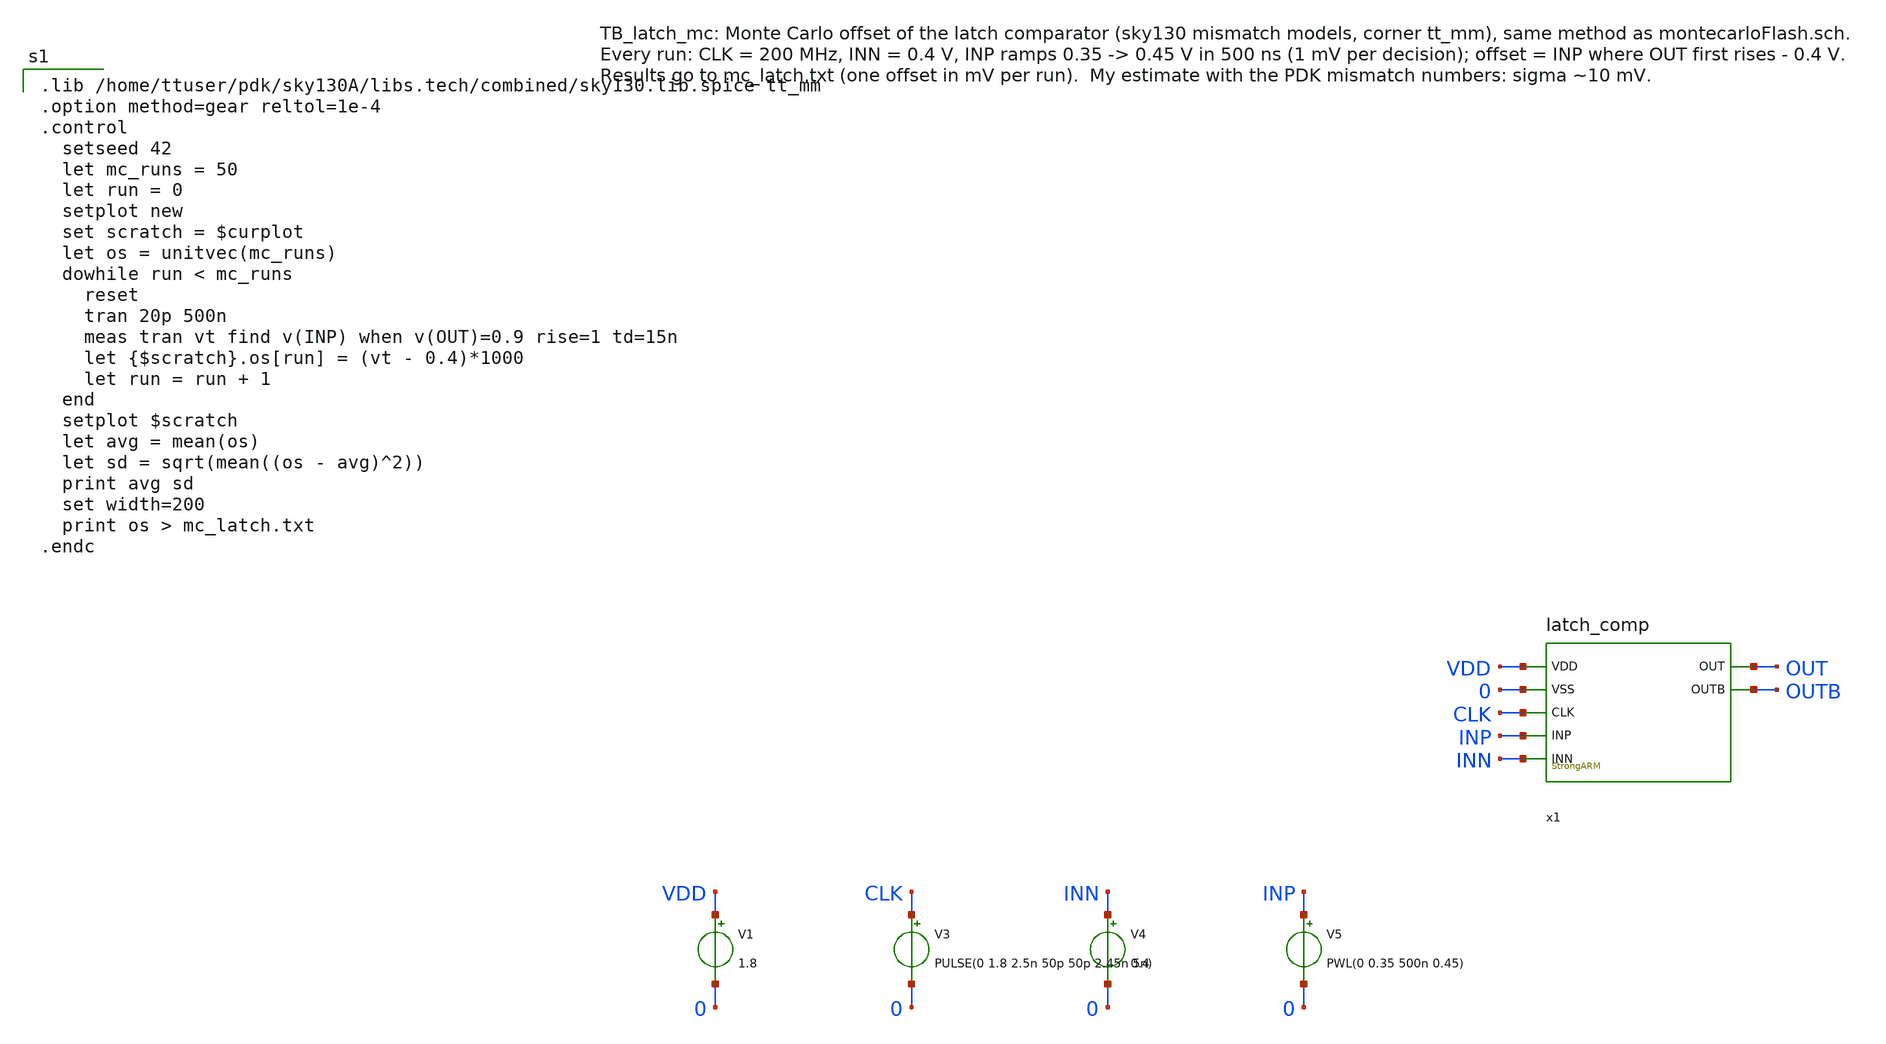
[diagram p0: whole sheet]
** sch_path: TB_latch_mc.sch
**.subckt TB_latch_mc
x1 VDD 0 CLK INP INN OUT OUTB latch_comp
V1 VDD 0 1.8
V3 CLK 0 PULSE(0 1.8 2.5n 50p 50p 2.45n 5n)
V4 INN 0 0.4
V5 INP 0 PWL(0 0.35 500n 0.45)
**** begin user architecture code

.lib /home/ttuser/pdk/sky130A/libs.tech/combined/sky130.lib.spice tt_mm
.option method=gear reltol=1e-4
.control
  setseed 42
  let mc_runs = 50
  let run = 0
  setplot new
  set scratch = $curplot
  let os = unitvec(mc_runs)
  dowhile run < mc_runs
    reset
    tran 20p 500n
    meas tran vt find v(INP) when v(OUT)=0.9 rise=1 td=15n
    let {$scratch}.os[run] = (vt - 0.4)*1000
    let run = run + 1
  end
  setplot $scratch
  let avg = mean(os)
  let sd = sqrt(mean((os - avg)^2))
  print avg sd
  set width=200
  print os > mc_latch.txt
.endc

**** end user architecture code
**.ends

* expanding   symbol:  /home/ttuser/Documents/ADCAnalogDesign/SAR_improved/latch_comp.sym # of
*+ pins=7
** sym_path: SAR_improved/latch_comp.sym
** sch_path: SAR_improved/latch_comp.sch
.subckt latch_comp VDD VSS CLK INP INN OUT OUTB
*.ipin VDD
*.ipin VSS
*.ipin CLK
*.ipin INP
*.ipin INN
*.opin OUT
*.opin OUTB
XM7 TAIL CLKB VDD VDD sky130_fd_pr__pfet_01v8 L=0.15 W=2 nf=1 ad='int((nf+1)/2) * W/nf * 0.29' as='int((nf+2)/2) * W/nf * 0.29'
+ pd='2*int((nf+1)/2) * (W/nf + 0.29)' ps='2*int((nf+2)/2) * (W/nf + 0.29)' nrd='0.29 / W' nrs='0.29 / W'
+ sa=0 sb=0 sd=0 mult=1 m=1
XM1 P INP TAIL VDD sky130_fd_pr__pfet_01v8 L=0.5 W=2 nf=1 ad='int((nf+1)/2) * W/nf * 0.29' as='int((nf+2)/2) * W/nf * 0.29'
+ pd='2*int((nf+1)/2) * (W/nf + 0.29)' ps='2*int((nf+2)/2) * (W/nf + 0.29)' nrd='0.29 / W' nrs='0.29 / W'
+ sa=0 sb=0 sd=0 mult=1 m=1
XM2 Q INN TAIL VDD sky130_fd_pr__pfet_01v8 L=0.5 W=2 nf=1 ad='int((nf+1)/2) * W/nf * 0.29' as='int((nf+2)/2) * W/nf * 0.29'
+ pd='2*int((nf+1)/2) * (W/nf + 0.29)' ps='2*int((nf+2)/2) * (W/nf + 0.29)' nrd='0.29 / W' nrs='0.29 / W'
+ sa=0 sb=0 sd=0 mult=1 m=1
XM3 X Y P VDD sky130_fd_pr__pfet_01v8 L=0.15 W=1 nf=1 ad='int((nf+1)/2) * W/nf * 0.29' as='int((nf+2)/2) * W/nf * 0.29'
+ pd='2*int((nf+1)/2) * (W/nf + 0.29)' ps='2*int((nf+2)/2) * (W/nf + 0.29)' nrd='0.29 / W' nrs='0.29 / W'
+ sa=0 sb=0 sd=0 mult=1 m=1
XM4 Y X Q VDD sky130_fd_pr__pfet_01v8 L=0.15 W=1 nf=1 ad='int((nf+1)/2) * W/nf * 0.29' as='int((nf+2)/2) * W/nf * 0.29'
+ pd='2*int((nf+1)/2) * (W/nf + 0.29)' ps='2*int((nf+2)/2) * (W/nf + 0.29)' nrd='0.29 / W' nrs='0.29 / W'
+ sa=0 sb=0 sd=0 mult=1 m=1
XM5 X Y VSS VSS sky130_fd_pr__nfet_01v8 L=0.15 W=0.5 nf=1 ad='int((nf+1)/2) * W/nf * 0.29' as='int((nf+2)/2) * W/nf * 0.29'
+ pd='2*int((nf+1)/2) * (W/nf + 0.29)' ps='2*int((nf+2)/2) * (W/nf + 0.29)' nrd='0.29 / W' nrs='0.29 / W'
+ sa=0 sb=0 sd=0 mult=1 m=1
XM6 Y X VSS VSS sky130_fd_pr__nfet_01v8 L=0.15 W=0.5 nf=1 ad='int((nf+1)/2) * W/nf * 0.29' as='int((nf+2)/2) * W/nf * 0.29'
+ pd='2*int((nf+1)/2) * (W/nf + 0.29)' ps='2*int((nf+2)/2) * (W/nf + 0.29)' nrd='0.29 / W' nrs='0.29 / W'
+ sa=0 sb=0 sd=0 mult=1 m=1
XMR1 P CLKB VSS VSS sky130_fd_pr__nfet_01v8 L=0.15 W=0.5 nf=1 ad='int((nf+1)/2) * W/nf * 0.29' as='int((nf+2)/2) * W/nf * 0.29'
+ pd='2*int((nf+1)/2) * (W/nf + 0.29)' ps='2*int((nf+2)/2) * (W/nf + 0.29)' nrd='0.29 / W' nrs='0.29 / W'
+ sa=0 sb=0 sd=0 mult=1 m=1
XMR2 Q CLKB VSS VSS sky130_fd_pr__nfet_01v8 L=0.15 W=0.5 nf=1 ad='int((nf+1)/2) * W/nf * 0.29' as='int((nf+2)/2) * W/nf * 0.29'
+ pd='2*int((nf+1)/2) * (W/nf + 0.29)' ps='2*int((nf+2)/2) * (W/nf + 0.29)' nrd='0.29 / W' nrs='0.29 / W'
+ sa=0 sb=0 sd=0 mult=1 m=1
XMR3 X CLKB VSS VSS sky130_fd_pr__nfet_01v8 L=0.15 W=0.5 nf=1 ad='int((nf+1)/2) * W/nf * 0.29' as='int((nf+2)/2) * W/nf * 0.29'
+ pd='2*int((nf+1)/2) * (W/nf + 0.29)' ps='2*int((nf+2)/2) * (W/nf + 0.29)' nrd='0.29 / W' nrs='0.29 / W'
+ sa=0 sb=0 sd=0 mult=1 m=1
XMR4 Y CLKB VSS VSS sky130_fd_pr__nfet_01v8 L=0.15 W=0.5 nf=1 ad='int((nf+1)/2) * W/nf * 0.29' as='int((nf+2)/2) * W/nf * 0.29'
+ pd='2*int((nf+1)/2) * (W/nf + 0.29)' ps='2*int((nf+2)/2) * (W/nf + 0.29)' nrd='0.29 / W' nrs='0.29 / W'
+ sa=0 sb=0 sd=0 mult=1 m=1
x1 YB OUTB OUT VDD VSS nand2
x2 XB OUT OUTB VDD VSS nand2
x3 VDD X XB VSS inverter
x4 VDD Y YB VSS inverter
x5 VDD CLK CLKB VSS inverter
.ends


* expanding   symbol:  /home/ttuser/Documents/ADCAnalogDesign/nand2.sym # of pins=5
** sym_path: nand2.sym
** sch_path: nand2.sch
.subckt nand2 A B Y VCC VSS
*.ipin A
*.ipin B
*.opin Y
*.iopin VCC
*.iopin VSS
XM1 Y A VCC VCC sky130_fd_pr__pfet_01v8 L=0.15 W=2 nf=1 ad='int((nf+1)/2) * W/nf * 0.29' as='int((nf+2)/2) * W/nf * 0.29'
+ pd='2*int((nf+1)/2) * (W/nf + 0.29)' ps='2*int((nf+2)/2) * (W/nf + 0.29)' nrd='0.29 / W' nrs='0.29 / W'
+ sa=0 sb=0 sd=0 mult=1 m=1
XM2 Y B VCC VCC sky130_fd_pr__pfet_01v8 L=0.15 W=2 nf=1 ad='int((nf+1)/2) * W/nf * 0.29' as='int((nf+2)/2) * W/nf * 0.29'
+ pd='2*int((nf+1)/2) * (W/nf + 0.29)' ps='2*int((nf+2)/2) * (W/nf + 0.29)' nrd='0.29 / W' nrs='0.29 / W'
+ sa=0 sb=0 sd=0 mult=1 m=1
XM3 Y A N1 VSS sky130_fd_pr__nfet_01v8 L=0.15 W=2 nf=1 ad='int((nf+1)/2) * W/nf * 0.29' as='int((nf+2)/2) * W/nf * 0.29'
+ pd='2*int((nf+1)/2) * (W/nf + 0.29)' ps='2*int((nf+2)/2) * (W/nf + 0.29)' nrd='0.29 / W' nrs='0.29 / W'
+ sa=0 sb=0 sd=0 mult=1 m=1
XM4 N1 B VSS VSS sky130_fd_pr__nfet_01v8 L=0.15 W=2 nf=1 ad='int((nf+1)/2) * W/nf * 0.29' as='int((nf+2)/2) * W/nf * 0.29'
+ pd='2*int((nf+1)/2) * (W/nf + 0.29)' ps='2*int((nf+2)/2) * (W/nf + 0.29)' nrd='0.29 / W' nrs='0.29 / W'
+ sa=0 sb=0 sd=0 mult=1 m=1
.ends


* expanding   symbol:  /home/ttuser/Documents/ADCAnalogDesign/inverter.sym # of pins=4
** sym_path: inverter.sym
** sch_path: inverter.sch
.subckt inverter VDD IN out VSS
*.ipin IN
*.opin out
*.iopin VDD
*.iopin VSS
XM3 out IN VDD VDD sky130_fd_pr__pfet_01v8 L=0.15 W=1 nf=1 ad='int((nf+1)/2) * W/nf * 0.29' as='int((nf+2)/2) * W/nf * 0.29'
+ pd='2*int((nf+1)/2) * (W/nf + 0.29)' ps='2*int((nf+2)/2) * (W/nf + 0.29)' nrd='0.29 / W' nrs='0.29 / W'
+ sa=0 sb=0 sd=0 mult=1 m=1
XM2 out IN VSS VSS sky130_fd_pr__nfet_01v8 L=0.15 W=1 nf=1 ad='int((nf+1)/2) * W/nf * 0.29' as='int((nf+2)/2) * W/nf * 0.29'
+ pd='2*int((nf+1)/2) * (W/nf + 0.29)' ps='2*int((nf+2)/2) * (W/nf + 0.29)' nrd='0.29 / W' nrs='0.29 / W'
+ sa=0 sb=0 sd=0 mult=1 m=1
.ends

.end
